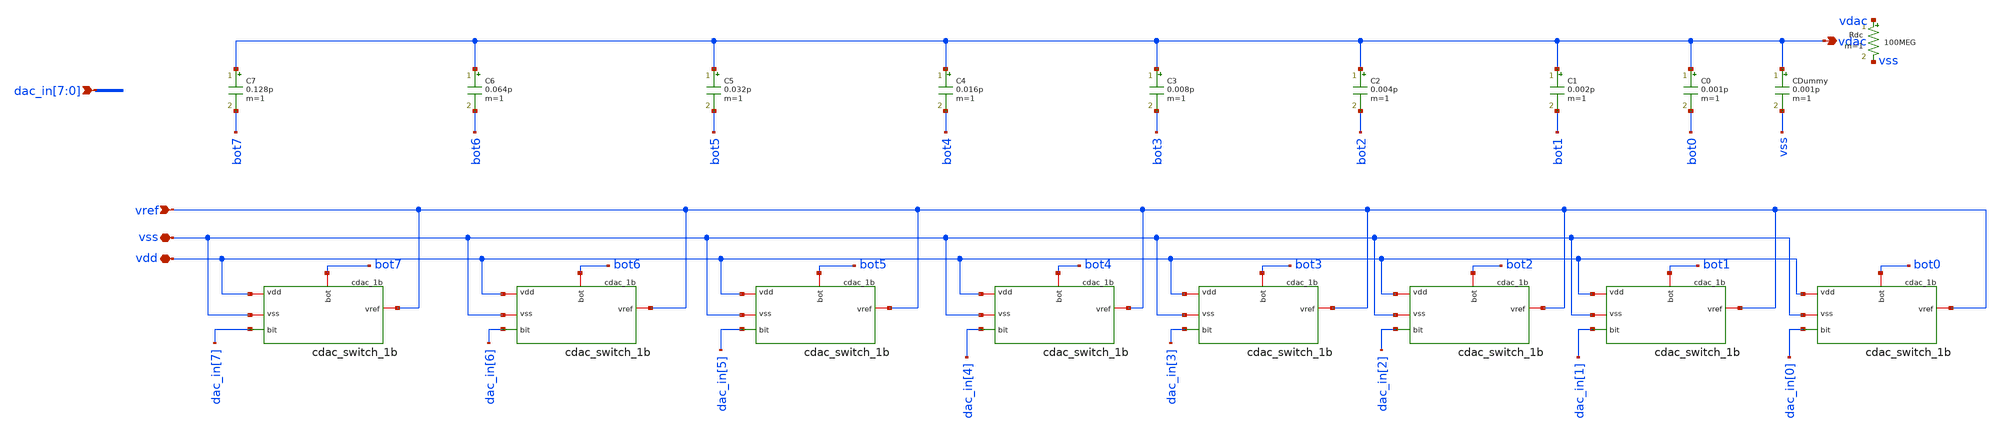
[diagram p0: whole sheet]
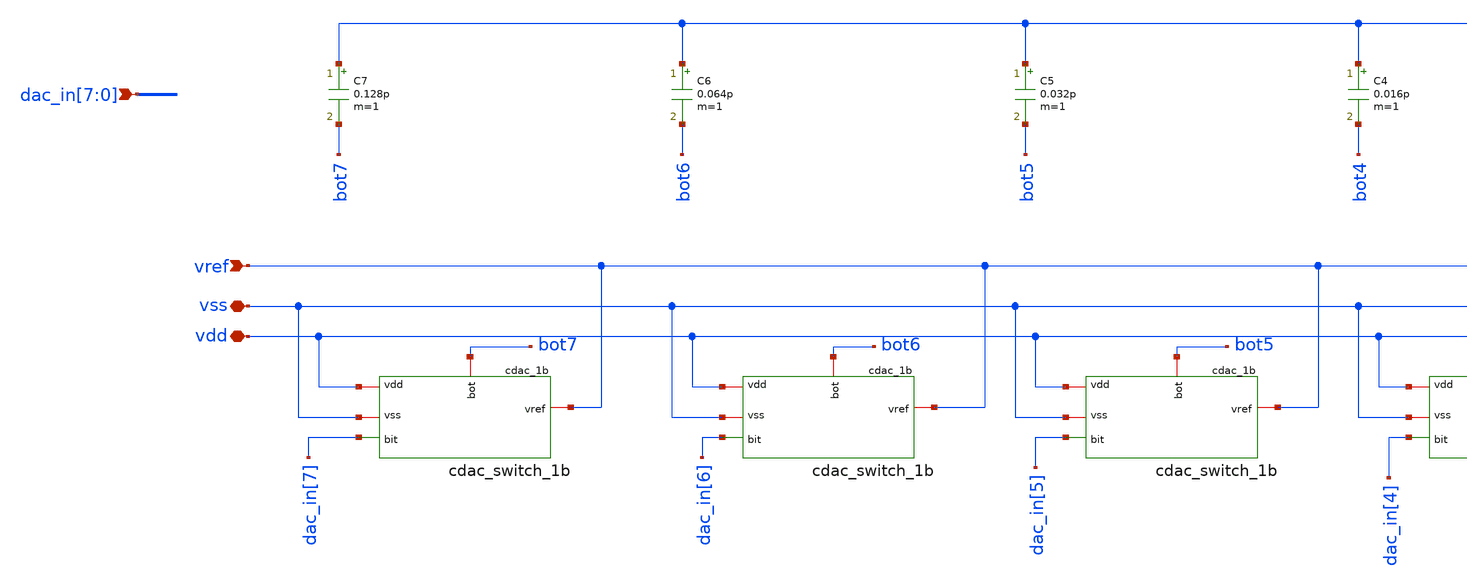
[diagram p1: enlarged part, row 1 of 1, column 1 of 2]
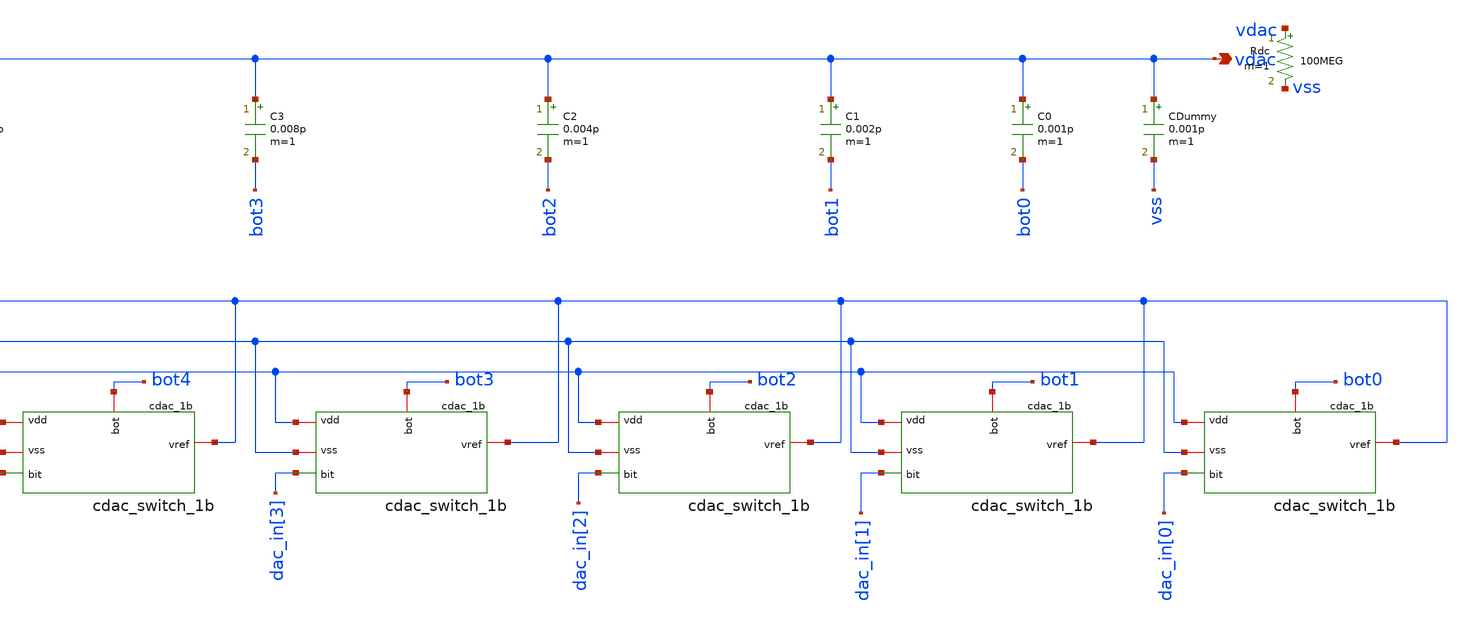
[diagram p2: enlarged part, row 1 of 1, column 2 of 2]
** sch_path: xschem/sar_adc/blocks/cdac/cdac_8bit.sch
**.subckt cdac_8bit vref vdd vss vdac
*+ dac_in[7],dac_in[6],dac_in[5],dac_in[4],dac_in[3],dac_in[2],dac_in[1],dac_in[0]
*.ipin vref
*.iopin vdd
*.iopin vss
*.opin vdac
*.ipin dac_in[7],dac_in[6],dac_in[5],dac_in[4],dac_in[3],dac_in[2],dac_in[1],dac_in[0]
C0 vdac bot0 0.001p m=1
C1 vdac bot1 0.002p m=1
C2 vdac bot2 0.004p m=1
C3 vdac bot3 0.008p m=1
C4 vdac bot4 0.016p m=1
C5 vdac bot5 0.032p m=1
C6 vdac bot6 0.064p m=1
C7 vdac bot7 0.128p m=1
XSW0 vref vdd vss bot0 dac_in[0] cdac_switch_1b
XSW1 vref vdd vss bot1 dac_in[1] cdac_switch_1b
XSW2 vref vdd vss bot2 dac_in[2] cdac_switch_1b
XSW3 vref vdd vss bot3 dac_in[3] cdac_switch_1b
XSW4 vref vdd vss bot4 dac_in[4] cdac_switch_1b
XSW5 vref vdd vss bot5 dac_in[5] cdac_switch_1b
XSW6 vref vdd vss bot6 dac_in[6] cdac_switch_1b
XSW7 vref vdd vss bot7 dac_in[7] cdac_switch_1b
CDummy vdac vss 0.001p m=1
Rdc vdac vss 100MEG m=1
**.ends

* expanding   symbol:  sar_adc/blocks/cdac/cdac_switch_1b.sym # of pins=5
** sym_path: xschem/sar_adc/blocks/cdac/cdac_switch_1b.sym
** sch_path: xschem/sar_adc/blocks/cdac/cdac_switch_1b.sch
.subckt cdac_switch_1b vref vdd vss bot bit
*.iopin vdd
*.iopin vss
*.iopin vref
*.ipin bit
*.iopin bot
*.iopin vdd
*.iopin vss
XM1 bit_b bit vdd vdd pfet_03v3 L=0.28u W=1u nf=1 ad='int((nf+1)/2) * W/nf * 0.18u' as='int((nf+2)/2) * W/nf * 0.18u'
+ pd='2*int((nf+1)/2) * (W/nf + 0.18u)' ps='2*int((nf+2)/2) * (W/nf + 0.18u)' nrd='0.18u / W' nrs='0.18u / W'
+ sa=0 sb=0 sd=0 m=1
XM2 bit_b bit vss vss nfet_03v3 L=0.28u W=0.5u nf=1 ad='int((nf+1)/2) * W/nf * 0.18u' as='int((nf+2)/2) * W/nf * 0.18u'
+ pd='2*int((nf+1)/2) * (W/nf + 0.18u)' ps='2*int((nf+2)/2) * (W/nf + 0.18u)' nrd='0.18u / W' nrs='0.18u / W'
+ sa=0 sb=0 sd=0 m=1
XM3 bot bit_b vref vdd pfet_03v3 L=0.28u W=20u nf=1 ad='int((nf+1)/2) * W/nf * 0.18u' as='int((nf+2)/2) * W/nf * 0.18u'
+ pd='2*int((nf+1)/2) * (W/nf + 0.18u)' ps='2*int((nf+2)/2) * (W/nf + 0.18u)' nrd='0.18u / W' nrs='0.18u / W'
+ sa=0 sb=0 sd=0 m=1
XM4 vref bit bot vss nfet_03v3 L=0.28u W=10u nf=1 ad='int((nf+1)/2) * W/nf * 0.18u' as='int((nf+2)/2) * W/nf * 0.18u'
+ pd='2*int((nf+1)/2) * (W/nf + 0.18u)' ps='2*int((nf+2)/2) * (W/nf + 0.18u)' nrd='0.18u / W' nrs='0.18u / W'
+ sa=0 sb=0 sd=0 m=1
XM5 bot bit vss vdd pfet_03v3 L=0.28u W=20u nf=1 ad='int((nf+1)/2) * W/nf * 0.18u' as='int((nf+2)/2) * W/nf * 0.18u'
+ pd='2*int((nf+1)/2) * (W/nf + 0.18u)' ps='2*int((nf+2)/2) * (W/nf + 0.18u)' nrd='0.18u / W' nrs='0.18u / W'
+ sa=0 sb=0 sd=0 m=1
XM6 vss bit_b bot vss nfet_03v3 L=0.28u W=10u nf=1 ad='int((nf+1)/2) * W/nf * 0.18u' as='int((nf+2)/2) * W/nf * 0.18u'
+ pd='2*int((nf+1)/2) * (W/nf + 0.18u)' ps='2*int((nf+2)/2) * (W/nf + 0.18u)' nrd='0.18u / W' nrs='0.18u / W'
+ sa=0 sb=0 sd=0 m=1
.ends

.end
